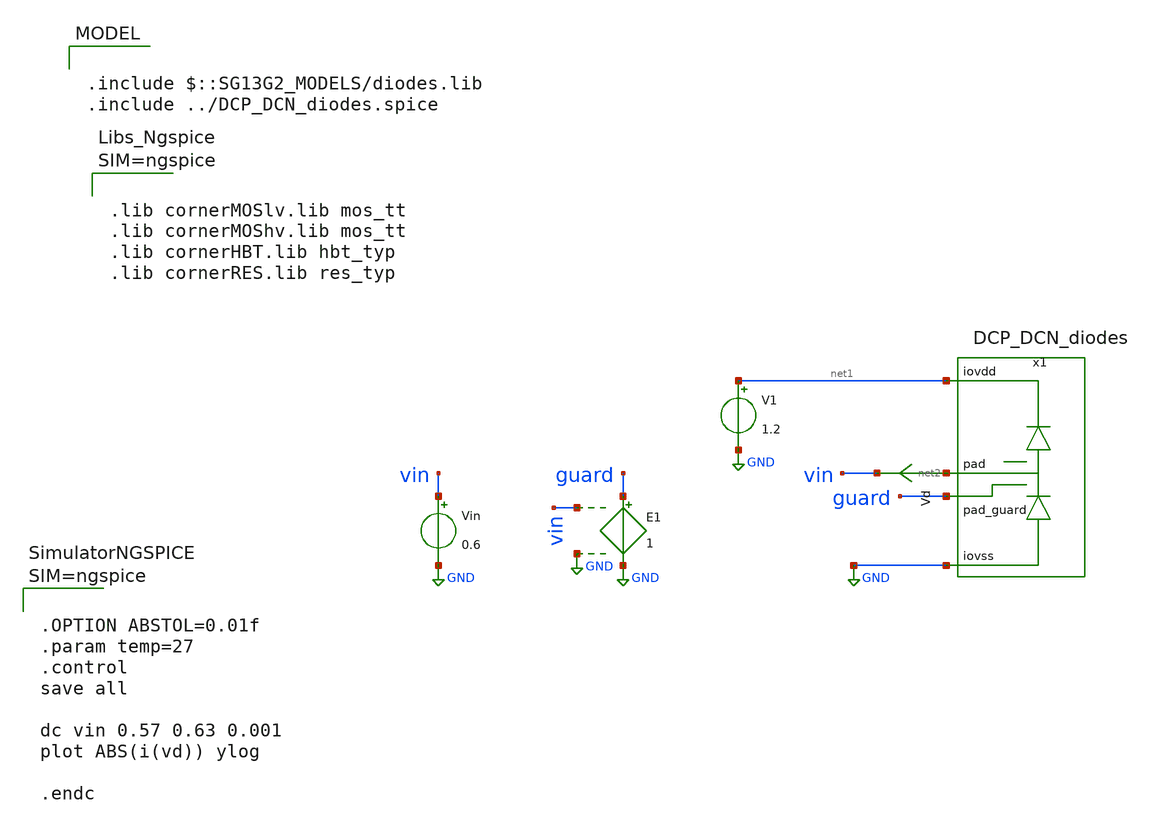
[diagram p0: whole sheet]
** sch_path: trident_test_structures/design_data/xschem/IOPadAnalog_submodules/DCP_DCN_diodes_tb.sch
**.subckt DCP_DCN_diodes_tb
Vd net2 vin 0
.save i(vd)
Vin vin GND 0.6
V1 net1 GND 1.2
E1 guard GND vin GND 1
x1 net1 net2 GND guard DCP_DCN_diodes
**** begin user architecture code



.lib cornerMOSlv.lib mos_tt
.lib cornerMOShv.lib mos_tt
.lib cornerHBT.lib hbt_typ
.lib cornerRES.lib res_typ






.OPTION ABSTOL=0.01f
.param temp=27
.control
save all

dc vin 0.57 0.63 0.001
plot ABS(i(vd)) ylog

.endc




.include $::SG13G2_MODELS/diodes.lib
.include ../DCP_DCN_diodes.spice

**** end user architecture code
**.ends
.GLOBAL GND
.end
